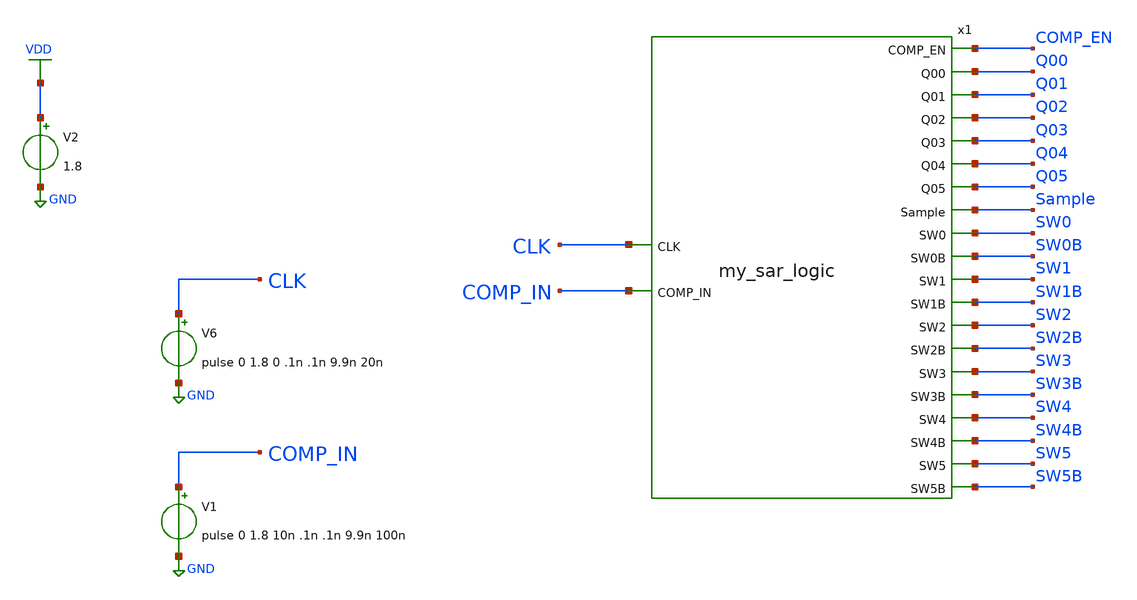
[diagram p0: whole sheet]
** sch_path: tb_my_logic.sch
**.subckt tb_my_logic
x1 SW3B SW4B SW1 SW2 SW0 SW3 SW0B SW1B SW2B SW5 SW5B SW4 Q03 Q04 Q00 Q05 Q01 Q02 COMP_IN Sample CLK
+ COMP_EN my_sar_logic
V6 CLK GND pulse 0 1.8 0 .1n .1n 9.9n 20n
V1 COMP_IN GND pulse 0 1.8 10n .1n .1n 9.9n 100n
V2 VDD GND 1.8
**** begin user architecture code
 .lib $::SKYWATER_MODELS/sky130.lib.spice tt
.include $::SKYWATER_STDCELLS/sky130_fd_sc_hd.spice



.options acct list
.temp 25

.tran 1n 1u
.control
.write tb_saradc.raw
.endc


**** end user architecture code
**.ends
.GLOBAL GND
.GLOBAL VDD
.end
